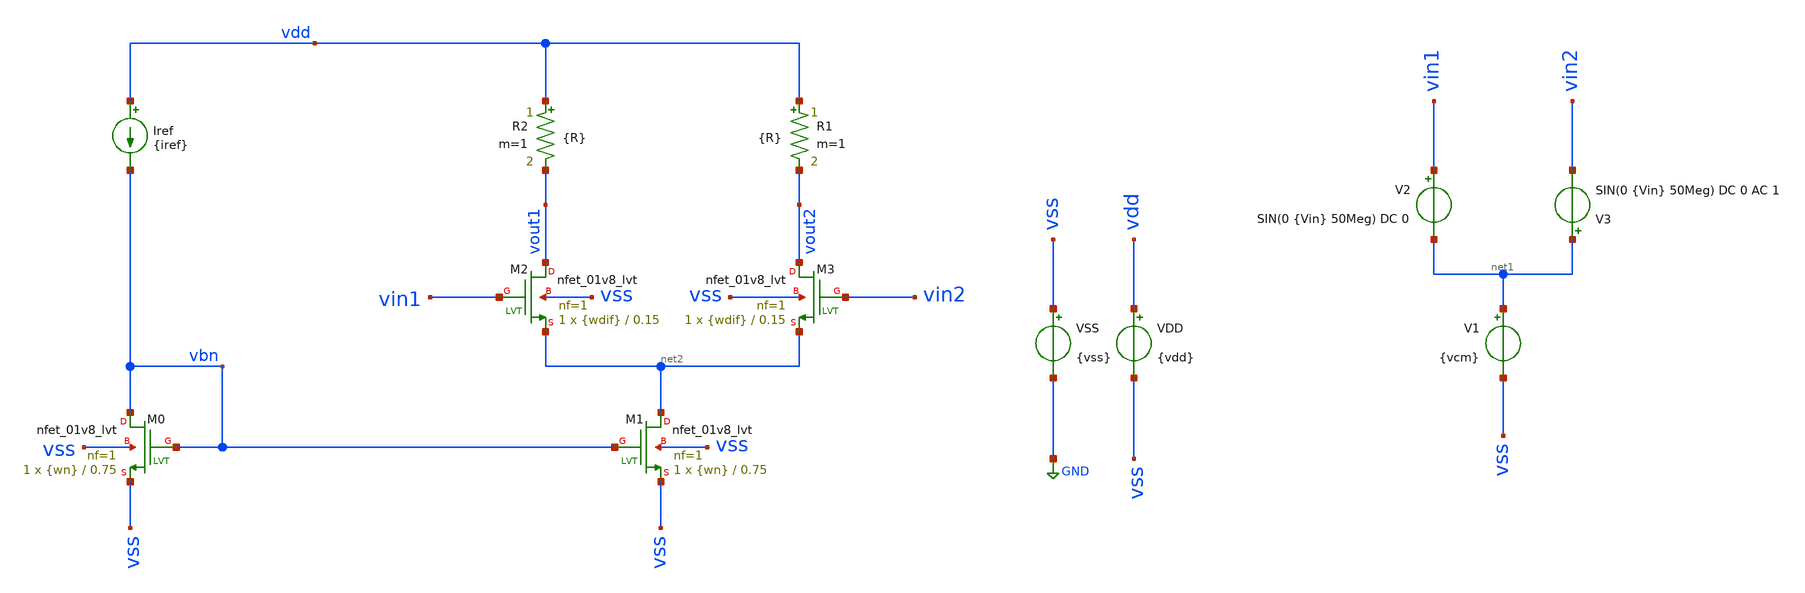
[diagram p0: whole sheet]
** sch_path: tp3/tp3_1.sch
**.subckt tp3_1
Iref vdd vbn {iref}
VSS vss GND {vss}
VDD vdd vss {vdd}
V1 net1 vss {vcm}
XM1 net2 vbn vss vss sky130_fd_pr__nfet_01v8_lvt L=0.75 W={wn} nf=1 ad='int((nf+1)/2) * W/nf * 0.29'
+ as='int((nf+2)/2) * W/nf * 0.29' pd='2*int((nf+1)/2) * (W/nf + 0.29)' ps='2*int((nf+2)/2) * (W/nf + 0.29)'
+ nrd='0.29 / W' nrs='0.29 / W' sa=0 sb=0 sd=0 mult=1 m=1
XM0 vbn vbn vss vss sky130_fd_pr__nfet_01v8_lvt L=0.75 W={wn} nf=1 ad='int((nf+1)/2) * W/nf * 0.29' as='int((nf+2)/2) * W/nf * 0.29'
+ pd='2*int((nf+1)/2) * (W/nf + 0.29)' ps='2*int((nf+2)/2) * (W/nf + 0.29)' nrd='0.29 / W' nrs='0.29 / W'
+ sa=0 sb=0 sd=0 mult=1 m=1
XM2 vout1 vin1 net2 vss sky130_fd_pr__nfet_01v8_lvt L=0.15 W={wdif} nf=1 ad='int((nf+1)/2) * W/nf * 0.29'
+ as='int((nf+2)/2) * W/nf * 0.29' pd='2*int((nf+1)/2) * (W/nf + 0.29)' ps='2*int((nf+2)/2) * (W/nf + 0.29)'
+ nrd='0.29 / W' nrs='0.29 / W' sa=0 sb=0 sd=0 mult=1 m=1
R2 vdd vout1 {R} m=1
XM3 vout2 vin2 net2 vss sky130_fd_pr__nfet_01v8_lvt L=0.15 W={wdif} nf=1 ad='int((nf+1)/2) * W/nf * 0.29'
+ as='int((nf+2)/2) * W/nf * 0.29' pd='2*int((nf+1)/2) * (W/nf + 0.29)' ps='2*int((nf+2)/2) * (W/nf + 0.29)'
+ nrd='0.29 / W' nrs='0.29 / W' sa=0 sb=0 sd=0 mult=1 m=1
R1 vdd vout2 {R} m=1
V2 vin1 net1 SIN(0 {Vin} 50Meg) DC 0
V3 net1 vin2 SIN(0 {Vin} 50Meg) DC 0 AC 1
**** begin user architecture code



* Parameters

.options TEMP = 65.0

* Models
.lib ~/skywater/skywater-pdk/libraries/sky130_fd_pr_ngspice/latest/models/corners/sky130.lib TT

* Data to save
.save all


* Simulation
.control

.endc

.end


**** end user architecture code
**.ends
.GLOBAL GND
.end
